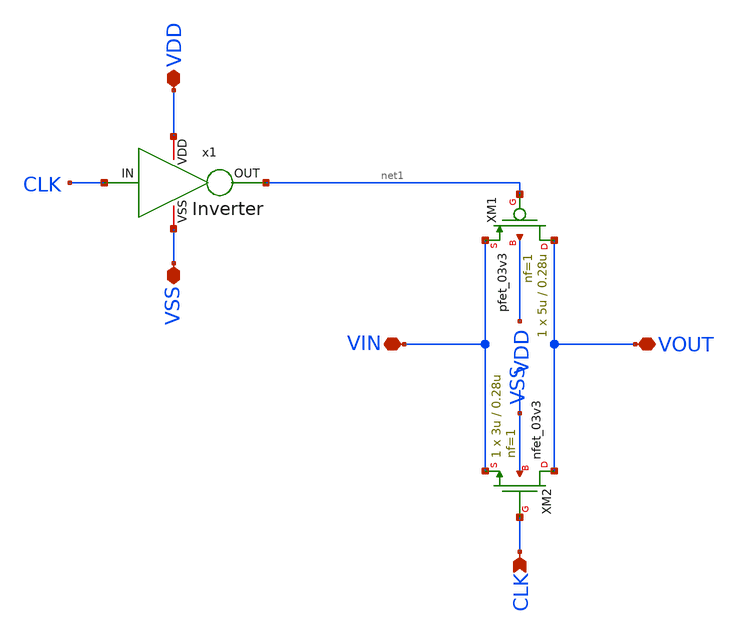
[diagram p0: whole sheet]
** sch_path: SCOP_INPUT_AND_MUX_PAKISTAN_03/Xschem/Logic_Gates/Transmission_Gate_5x.sch
**.subckt Transmission_Gate_5x VDD VSS VOUT CLK VIN
*.iopin VDD
*.iopin VSS
*.iopin VOUT
*.ipin CLK
*.iopin VIN
XM1 VOUT net1 VIN VDD pfet_03v3 L=0.28u W=5u nf=1 ad='int((nf+1)/2) * W/nf * 0.18u' as='int((nf+2)/2) * W/nf * 0.18u'
+ pd='2*int((nf+1)/2) * (W/nf + 0.18u)' ps='2*int((nf+2)/2) * (W/nf + 0.18u)' nrd='0.18u / W' nrs='0.18u / W'
+ sa=0 sb=0 sd=0 m=1
XM2 VOUT CLK VIN VSS nfet_03v3 L=0.28u W=3u nf=1 ad='int((nf+1)/2) * W/nf * 0.18u' as='int((nf+2)/2) * W/nf * 0.18u'
+ pd='2*int((nf+1)/2) * (W/nf + 0.18u)' ps='2*int((nf+2)/2) * (W/nf + 0.18u)' nrd='0.18u / W' nrs='0.18u / W'
+ sa=0 sb=0 sd=0 m=1
x1 VDD net1 CLK VSS Inverter
**.ends
.end
